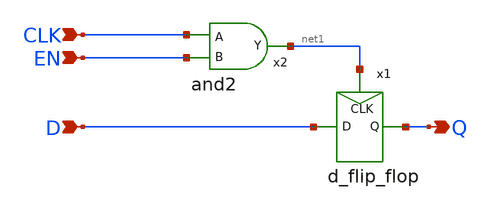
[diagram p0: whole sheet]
** sch_path: xschem/register.sch
**.subckt register CLK EN D Q
*.ipin CLK
*.ipin EN
*.ipin D
*.opin Q
x1 net1 Q D d_flip_flop
x2 CLK net1 EN and2
**.ends

* expanding   symbol:  d_flip_flop.sym # of pins=3
** sym_path: xschem/d_flip_flop.sym
** sch_path: xschem/d_flip_flop.sch
.subckt d_flip_flop CLK Q D
*.ipin CLK
*.ipin D
*.opin Q
XM1 CLK_n CLK gnd GND sky130_fd_pr__nfet_01v8 L=0.15 W=0.84 nf=1 ad='int((nf+1)/2) * W/nf * 0.29' as='int((nf+2)/2) * W/nf * 0.29'
+ pd='2*int((nf+1)/2) * (W/nf + 0.29)' ps='2*int((nf+2)/2) * (W/nf + 0.29)' nrd='0.29 / W' nrs='0.29 / W'
+ sa=0 sb=0 sd=0 mult=1 m=1
XM2 CLK_n CLK vdd VDD sky130_fd_pr__pfet_01v8 L=0.15 W=1.68 nf=1 ad='int((nf+1)/2) * W/nf * 0.29' as='int((nf+2)/2) * W/nf * 0.29'
+ pd='2*int((nf+1)/2) * (W/nf + 0.29)' ps='2*int((nf+2)/2) * (W/nf + 0.29)' nrd='0.29 / W' nrs='0.29 / W'
+ sa=0 sb=0 sd=0 mult=1 m=1
XM3 common_1 CLK net4 VDD sky130_fd_pr__pfet_01v8 L=0.15 W=0.42 nf=1 ad='int((nf+1)/2) * W/nf * 0.29'
+ as='int((nf+2)/2) * W/nf * 0.29' pd='2*int((nf+1)/2) * (W/nf + 0.29)' ps='2*int((nf+2)/2) * (W/nf + 0.29)'
+ nrd='0.29 / W' nrs='0.29 / W' sa=0 sb=0 sd=0 mult=1 m=1
XM4 net4 D vdd VDD sky130_fd_pr__pfet_01v8 L=0.15 W=0.42 nf=1 ad='int((nf+1)/2) * W/nf * 0.29' as='int((nf+2)/2) * W/nf * 0.29'
+ pd='2*int((nf+1)/2) * (W/nf + 0.29)' ps='2*int((nf+2)/2) * (W/nf + 0.29)' nrd='0.29 / W' nrs='0.29 / W'
+ sa=0 sb=0 sd=0 mult=1 m=1
XM5 common_1 CLK_n net3 GND sky130_fd_pr__nfet_01v8 L=0.15 W=0.42 nf=1 ad='int((nf+1)/2) * W/nf * 0.29'
+ as='int((nf+2)/2) * W/nf * 0.29' pd='2*int((nf+1)/2) * (W/nf + 0.29)' ps='2*int((nf+2)/2) * (W/nf + 0.29)'
+ nrd='0.29 / W' nrs='0.29 / W' sa=0 sb=0 sd=0 mult=1 m=1
XM6 net3 D gnd GND sky130_fd_pr__nfet_01v8 L=0.15 W=0.42 nf=1 ad='int((nf+1)/2) * W/nf * 0.29' as='int((nf+2)/2) * W/nf * 0.29'
+ pd='2*int((nf+1)/2) * (W/nf + 0.29)' ps='2*int((nf+2)/2) * (W/nf + 0.29)' nrd='0.29 / W' nrs='0.29 / W'
+ sa=0 sb=0 sd=0 mult=1 m=1
XM7 inverter_1_out common_1 vdd VDD sky130_fd_pr__pfet_01v8 L=0.15 W=0.42 nf=1 ad='int((nf+1)/2) * W/nf * 0.29'
+ as='int((nf+2)/2) * W/nf * 0.29' pd='2*int((nf+1)/2) * (W/nf + 0.29)' ps='2*int((nf+2)/2) * (W/nf + 0.29)'
+ nrd='0.29 / W' nrs='0.29 / W' sa=0 sb=0 sd=0 mult=1 m=1
XM8 inverter_1_out common_1 gnd GND sky130_fd_pr__nfet_01v8 L=0.15 W=0.42 nf=1 ad='int((nf+1)/2) * W/nf * 0.29'
+ as='int((nf+2)/2) * W/nf * 0.29' pd='2*int((nf+1)/2) * (W/nf + 0.29)' ps='2*int((nf+2)/2) * (W/nf + 0.29)'
+ nrd='0.29 / W' nrs='0.29 / W' sa=0 sb=0 sd=0 mult=1 m=1
XM9 common_1 CLK_n net2 VDD sky130_fd_pr__pfet_01v8 L=0.15 W=0.42 nf=1 ad='int((nf+1)/2) * W/nf * 0.29'
+ as='int((nf+2)/2) * W/nf * 0.29' pd='2*int((nf+1)/2) * (W/nf + 0.29)' ps='2*int((nf+2)/2) * (W/nf + 0.29)'
+ nrd='0.29 / W' nrs='0.29 / W' sa=0 sb=0 sd=0 mult=1 m=1
XM10 net2 inverter_1_out vdd VDD sky130_fd_pr__pfet_01v8 L=0.15 W=0.42 nf=1 ad='int((nf+1)/2) * W/nf * 0.29'
+ as='int((nf+2)/2) * W/nf * 0.29' pd='2*int((nf+1)/2) * (W/nf + 0.29)' ps='2*int((nf+2)/2) * (W/nf + 0.29)'
+ nrd='0.29 / W' nrs='0.29 / W' sa=0 sb=0 sd=0 mult=1 m=1
XM11 common_1 CLK net1 GND sky130_fd_pr__nfet_01v8 L=0.15 W=0.42 nf=1 ad='int((nf+1)/2) * W/nf * 0.29'
+ as='int((nf+2)/2) * W/nf * 0.29' pd='2*int((nf+1)/2) * (W/nf + 0.29)' ps='2*int((nf+2)/2) * (W/nf + 0.29)'
+ nrd='0.29 / W' nrs='0.29 / W' sa=0 sb=0 sd=0 mult=1 m=1
XM12 net1 inverter_1_out gnd GND sky130_fd_pr__nfet_01v8 L=0.15 W=0.42 nf=1 ad='int((nf+1)/2) * W/nf * 0.29'
+ as='int((nf+2)/2) * W/nf * 0.29' pd='2*int((nf+1)/2) * (W/nf + 0.29)' ps='2*int((nf+2)/2) * (W/nf + 0.29)'
+ nrd='0.29 / W' nrs='0.29 / W' sa=0 sb=0 sd=0 mult=1 m=1
XM13 common_2 CLK_n net6 VDD sky130_fd_pr__pfet_01v8 L=0.15 W=0.42 nf=1 ad='int((nf+1)/2) * W/nf * 0.29'
+ as='int((nf+2)/2) * W/nf * 0.29' pd='2*int((nf+1)/2) * (W/nf + 0.29)' ps='2*int((nf+2)/2) * (W/nf + 0.29)'
+ nrd='0.29 / W' nrs='0.29 / W' sa=0 sb=0 sd=0 mult=1 m=1
XM14 net6 inverter_1_out vdd VDD sky130_fd_pr__pfet_01v8 L=0.15 W=0.42 nf=1 ad='int((nf+1)/2) * W/nf * 0.29'
+ as='int((nf+2)/2) * W/nf * 0.29' pd='2*int((nf+1)/2) * (W/nf + 0.29)' ps='2*int((nf+2)/2) * (W/nf + 0.29)'
+ nrd='0.29 / W' nrs='0.29 / W' sa=0 sb=0 sd=0 mult=1 m=1
XM15 common_2 CLK net5 GND sky130_fd_pr__nfet_01v8 L=0.15 W=0.42 nf=1 ad='int((nf+1)/2) * W/nf * 0.29'
+ as='int((nf+2)/2) * W/nf * 0.29' pd='2*int((nf+1)/2) * (W/nf + 0.29)' ps='2*int((nf+2)/2) * (W/nf + 0.29)'
+ nrd='0.29 / W' nrs='0.29 / W' sa=0 sb=0 sd=0 mult=1 m=1
XM16 net5 inverter_1_out gnd GND sky130_fd_pr__nfet_01v8 L=0.15 W=0.42 nf=1 ad='int((nf+1)/2) * W/nf * 0.29'
+ as='int((nf+2)/2) * W/nf * 0.29' pd='2*int((nf+1)/2) * (W/nf + 0.29)' ps='2*int((nf+2)/2) * (W/nf + 0.29)'
+ nrd='0.29 / W' nrs='0.29 / W' sa=0 sb=0 sd=0 mult=1 m=1
XM17 Q common_2 vdd VDD sky130_fd_pr__pfet_01v8 L=0.15 W=0.84 nf=1 ad='int((nf+1)/2) * W/nf * 0.29' as='int((nf+2)/2) * W/nf * 0.29'
+ pd='2*int((nf+1)/2) * (W/nf + 0.29)' ps='2*int((nf+2)/2) * (W/nf + 0.29)' nrd='0.29 / W' nrs='0.29 / W'
+ sa=0 sb=0 sd=0 mult=1 m=1
XM18 Q common_2 gnd GND sky130_fd_pr__nfet_01v8 L=0.15 W=0.42 nf=1 ad='int((nf+1)/2) * W/nf * 0.29' as='int((nf+2)/2) * W/nf * 0.29'
+ pd='2*int((nf+1)/2) * (W/nf + 0.29)' ps='2*int((nf+2)/2) * (W/nf + 0.29)' nrd='0.29 / W' nrs='0.29 / W'
+ sa=0 sb=0 sd=0 mult=1 m=1
XM19 common_2 CLK net8 VDD sky130_fd_pr__pfet_01v8 L=0.15 W=0.42 nf=1 ad='int((nf+1)/2) * W/nf * 0.29'
+ as='int((nf+2)/2) * W/nf * 0.29' pd='2*int((nf+1)/2) * (W/nf + 0.29)' ps='2*int((nf+2)/2) * (W/nf + 0.29)'
+ nrd='0.29 / W' nrs='0.29 / W' sa=0 sb=0 sd=0 mult=1 m=1
XM20 net8 Q vdd VDD sky130_fd_pr__pfet_01v8 L=0.15 W=0.42 nf=1 ad='int((nf+1)/2) * W/nf * 0.29' as='int((nf+2)/2) * W/nf * 0.29'
+ pd='2*int((nf+1)/2) * (W/nf + 0.29)' ps='2*int((nf+2)/2) * (W/nf + 0.29)' nrd='0.29 / W' nrs='0.29 / W'
+ sa=0 sb=0 sd=0 mult=1 m=1
XM21 common_2 CLK_n net7 GND sky130_fd_pr__nfet_01v8 L=0.15 W=0.42 nf=1 ad='int((nf+1)/2) * W/nf * 0.29'
+ as='int((nf+2)/2) * W/nf * 0.29' pd='2*int((nf+1)/2) * (W/nf + 0.29)' ps='2*int((nf+2)/2) * (W/nf + 0.29)'
+ nrd='0.29 / W' nrs='0.29 / W' sa=0 sb=0 sd=0 mult=1 m=1
XM22 net7 Q gnd GND sky130_fd_pr__nfet_01v8 L=0.15 W=0.42 nf=1 ad='int((nf+1)/2) * W/nf * 0.29' as='int((nf+2)/2) * W/nf * 0.29'
+ pd='2*int((nf+1)/2) * (W/nf + 0.29)' ps='2*int((nf+2)/2) * (W/nf + 0.29)' nrd='0.29 / W' nrs='0.29 / W'
+ sa=0 sb=0 sd=0 mult=1 m=1
.ends


* expanding   symbol:  and2.sym # of pins=3
** sym_path: xschem/and2.sym
** sch_path: xschem/and2.sch
.subckt and2 A Y B
*.ipin A
*.ipin B
*.opin Y
XM1 net1 A net2 GND sky130_fd_pr__nfet_01v8 L=0.15 W=0.84 nf=1 ad='int((nf+1)/2) * W/nf * 0.29' as='int((nf+2)/2) * W/nf * 0.29'
+ pd='2*int((nf+1)/2) * (W/nf + 0.29)' ps='2*int((nf+2)/2) * (W/nf + 0.29)' nrd='0.29 / W' nrs='0.29 / W'
+ sa=0 sb=0 sd=0 mult=1 m=1
XM2 net2 B gnd GND sky130_fd_pr__nfet_01v8 L=0.15 W=0.84 nf=1 ad='int((nf+1)/2) * W/nf * 0.29' as='int((nf+2)/2) * W/nf * 0.29'
+ pd='2*int((nf+1)/2) * (W/nf + 0.29)' ps='2*int((nf+2)/2) * (W/nf + 0.29)' nrd='0.29 / W' nrs='0.29 / W'
+ sa=0 sb=0 sd=0 mult=1 m=1
XM3 net1 B vdd VDD sky130_fd_pr__pfet_01v8 L=0.15 W=0.84 nf=1 ad='int((nf+1)/2) * W/nf * 0.29' as='int((nf+2)/2) * W/nf * 0.29'
+ pd='2*int((nf+1)/2) * (W/nf + 0.29)' ps='2*int((nf+2)/2) * (W/nf + 0.29)' nrd='0.29 / W' nrs='0.29 / W'
+ sa=0 sb=0 sd=0 mult=1 m=1
XM4 net1 A vdd VDD sky130_fd_pr__pfet_01v8 L=0.15 W=0.84 nf=1 ad='int((nf+1)/2) * W/nf * 0.29' as='int((nf+2)/2) * W/nf * 0.29'
+ pd='2*int((nf+1)/2) * (W/nf + 0.29)' ps='2*int((nf+2)/2) * (W/nf + 0.29)' nrd='0.29 / W' nrs='0.29 / W'
+ sa=0 sb=0 sd=0 mult=1 m=1
XM5 Y net1 vdd VDD sky130_fd_pr__pfet_01v8 L=0.15 W=0.84 nf=1 ad='int((nf+1)/2) * W/nf * 0.29' as='int((nf+2)/2) * W/nf * 0.29'
+ pd='2*int((nf+1)/2) * (W/nf + 0.29)' ps='2*int((nf+2)/2) * (W/nf + 0.29)' nrd='0.29 / W' nrs='0.29 / W'
+ sa=0 sb=0 sd=0 mult=1 m=1
XM6 Y net1 gnd GND sky130_fd_pr__nfet_01v8 L=0.15 W=0.42 nf=1 ad='int((nf+1)/2) * W/nf * 0.29' as='int((nf+2)/2) * W/nf * 0.29'
+ pd='2*int((nf+1)/2) * (W/nf + 0.29)' ps='2*int((nf+2)/2) * (W/nf + 0.29)' nrd='0.29 / W' nrs='0.29 / W'
+ sa=0 sb=0 sd=0 mult=1 m=1
.ends

.GLOBAL vdd
.GLOBAL gnd
.end
